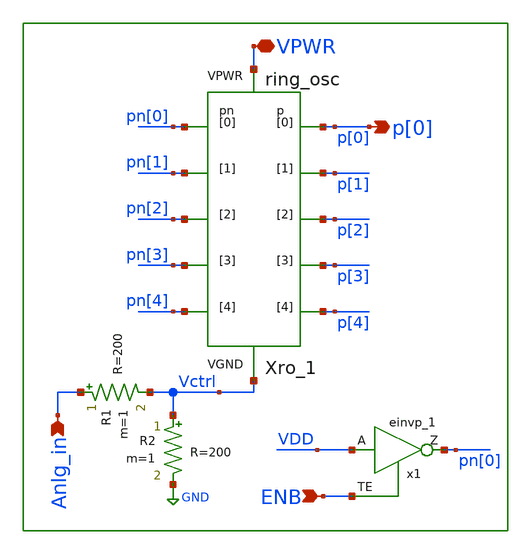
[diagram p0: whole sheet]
** sch_path: xschem/lib/AnalogLib_VCO.sch
**.subckt AnalogLib_VCO Anlg_in VPWR p[0] ENB
*.ipin Anlg_in
*.iopin VPWR
*.opin p[0]
*.ipin ENB
x1 VDD ENB VGND VNB VPB VPWR pn[0] sky130_fd_sc_ms__einvp_1
Xro_1 Vctrl VPWR p[0] p[1] p[2] p[3] p[4] pn[0] pn[1] pn[2] pn[3] pn[4] ring_osc L12="L12"
+ Wp12="Wp12" Wn12="Wn12" L34="L34" Wp34="Wp34" Wn34="Wn34"
R2 Vctrl GND R=200 m=1
R1 Anlg_in Vctrl R=200 m=1
**.ends
.GLOBAL GND
.end
